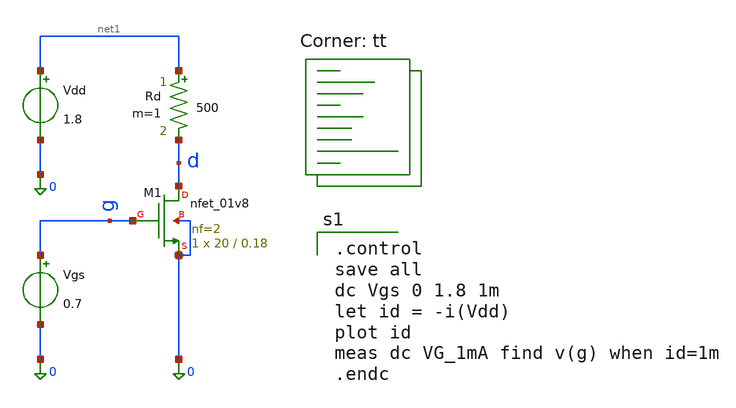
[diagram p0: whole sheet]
** sch_path: Homework 6 - Simulation on Open Source Softwares/Simulations/ex1_vgs.sch
**.subckt ex1_vgs
XM1 d g 0 0 sky130_fd_pr__nfet_01v8 L=0.18 W=20 nf=2 ad='int((2 + 1)/2) * 20 / 2 * 0.29' as='int((2 + 2)/2) * 20 / 2 * 0.29'
+ pd='2*int((2 + 1)/2) * (20 / 2 + 0.29)' ps='2*int((2 + 2)/2) * (20 / 2 + 0.29)' nrd='0.29 / 20 ' nrs='0.29 / 20 '
+ sa=0 sb=0 sd=0 mult=1 m=1
Vdd net1 0 1.8
Rd net1 d 500 m=1
Vgs g 0 0.7
**** begin user architecture code
.lib $::SKYWATER_MODELS/sky130.lib.spice tt

.control
save all
dc Vgs 0 1.8 1m
let id = -i(Vdd)
plot id
meas dc VG_1mA find v(g) when id=1m
.endc

**** end user architecture code
**.ends
.end
